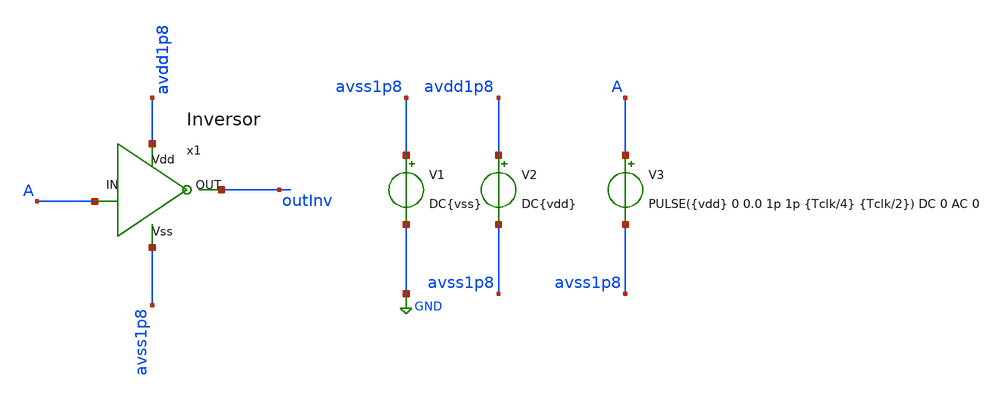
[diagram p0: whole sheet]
** sch_path: icdesign/sch/inv/Ej4.sch
**.subckt Ej4
V1 avss1p8 GND DC{vss}
V2 avdd1p8 avss1p8 DC{vdd}
V3 A avss1p8 PULSE({vdd} 0 0.0 1p 1p {Tclk/4} {Tclk/2}) DC 0 AC 0
x1 avdd1p8 A outInv avss1p8 Inversor
**** begin user architecture code





* Circuit Parameters
.param vdd  = 1.8
.param vss  = 0.0
.param Tclk = 10n
.options TEMP = 65.0


* Include Models
.lib ~/skywater/skywater-pdk/libraries/sky130_fd_pr_ngspice/latest/models/corners/sky130.lib TT


* OP Parameters & Singals to save
.save all


*Simulations
.control
  tran 0.01u 100n
  setplot tran1
  plot v(A) v(outInv)+2
.endc
.end


**** end user architecture code
**.ends

* expanding   symbol:  inv/Inversor.sym # of pins=4
** sym_path: icdesign/sch/inv/Inversor.sym
** sch_path: icdesign/sch/inv/Inversor.sch
.subckt Inversor Vdd IN OUT Vss
*.ipin IN
*.ipin Vdd
*.ipin Vss
*.opin OUT
XM1 OUT IN Vss Vss sky130_fd_pr__nfet_01v8 L=0.15 W=0.45 nf=1 ad='int((nf+1)/2) * W/nf * 0.29' as='int((nf+2)/2) * W/nf * 0.29'
+ pd='2*int((nf+1)/2) * (W/nf + 0.29)' ps='2*int((nf+2)/2) * (W/nf + 0.29)' nrd='0.29 / W' nrs='0.29 / W'
+ sa=0 sb=0 sd=0 mult=1 m=1
XM2 OUT IN Vdd Vdd sky130_fd_pr__pfet_01v8 L=0.15 W=0.45 nf=1 ad='int((nf+1)/2) * W/nf * 0.29' as='int((nf+2)/2) * W/nf * 0.29'
+ pd='2*int((nf+1)/2) * (W/nf + 0.29)' ps='2*int((nf+2)/2) * (W/nf + 0.29)' nrd='0.29 / W' nrs='0.29 / W'
+ sa=0 sb=0 sd=0 mult=1 m=1
.ends

.GLOBAL GND
.end
